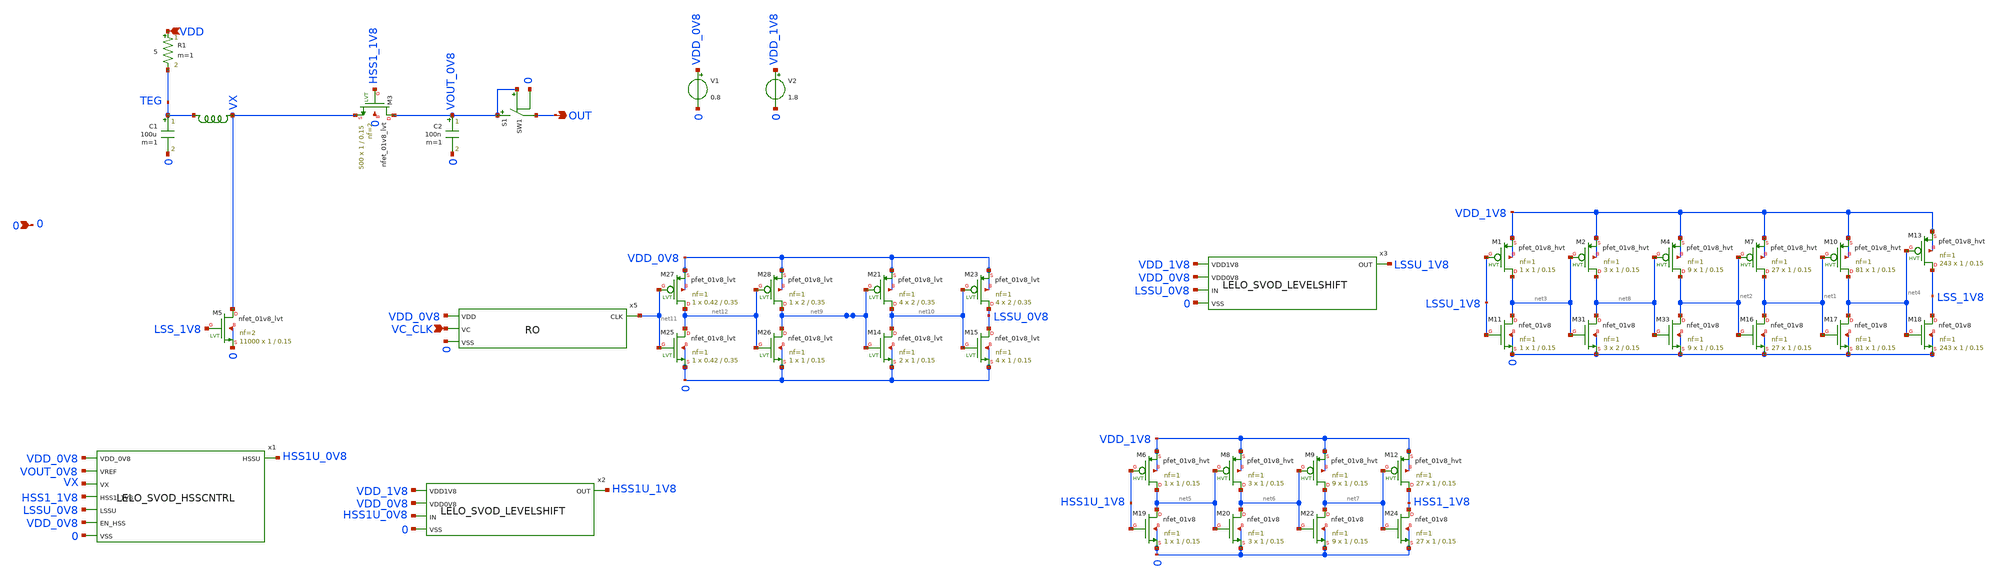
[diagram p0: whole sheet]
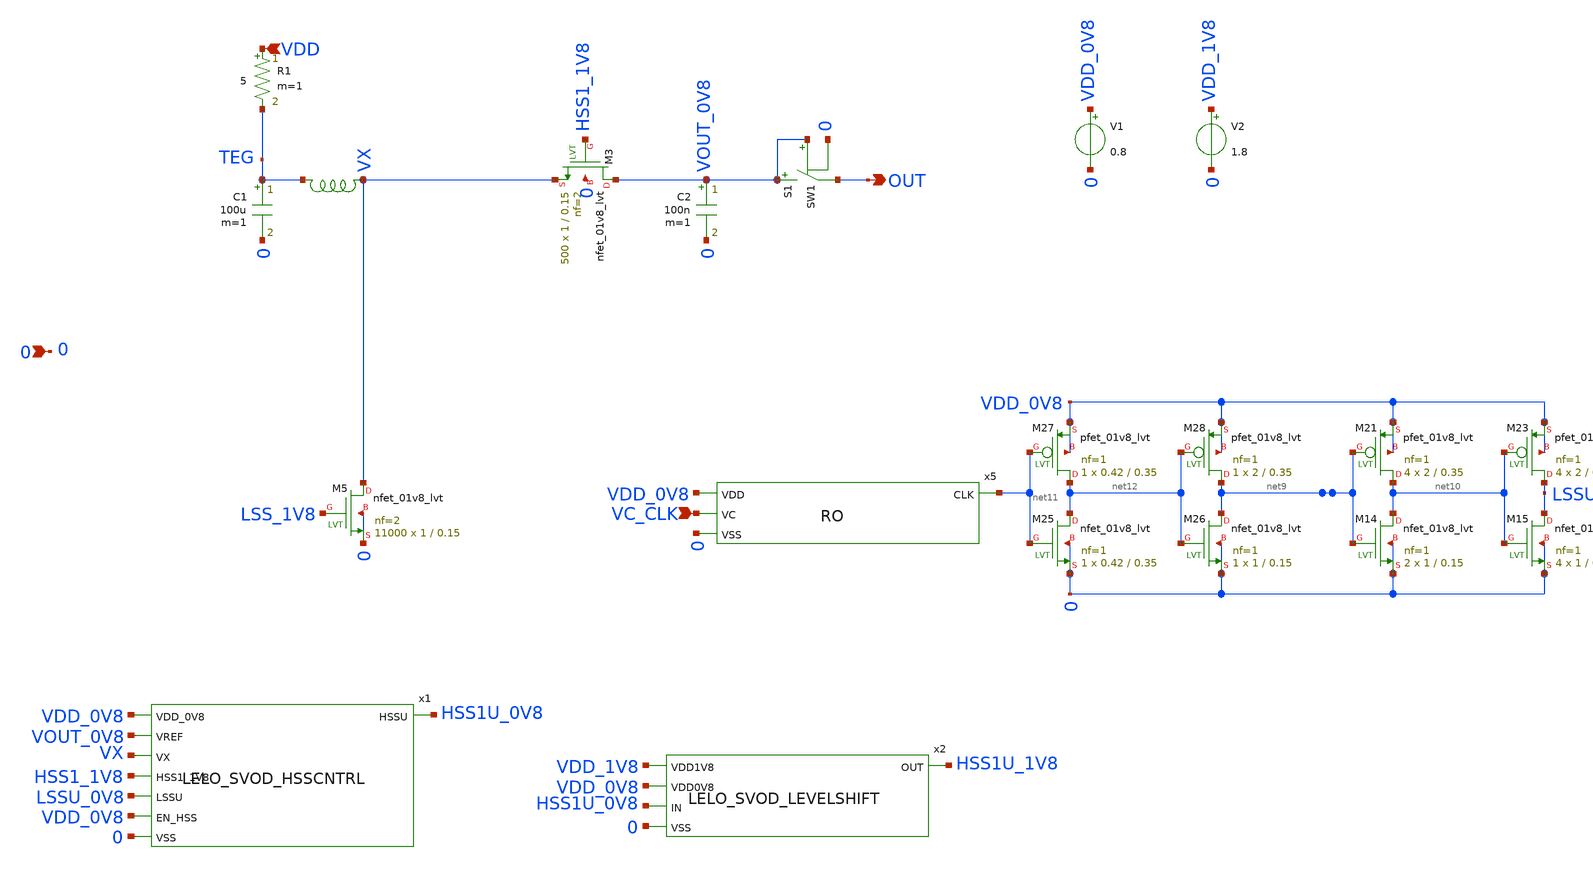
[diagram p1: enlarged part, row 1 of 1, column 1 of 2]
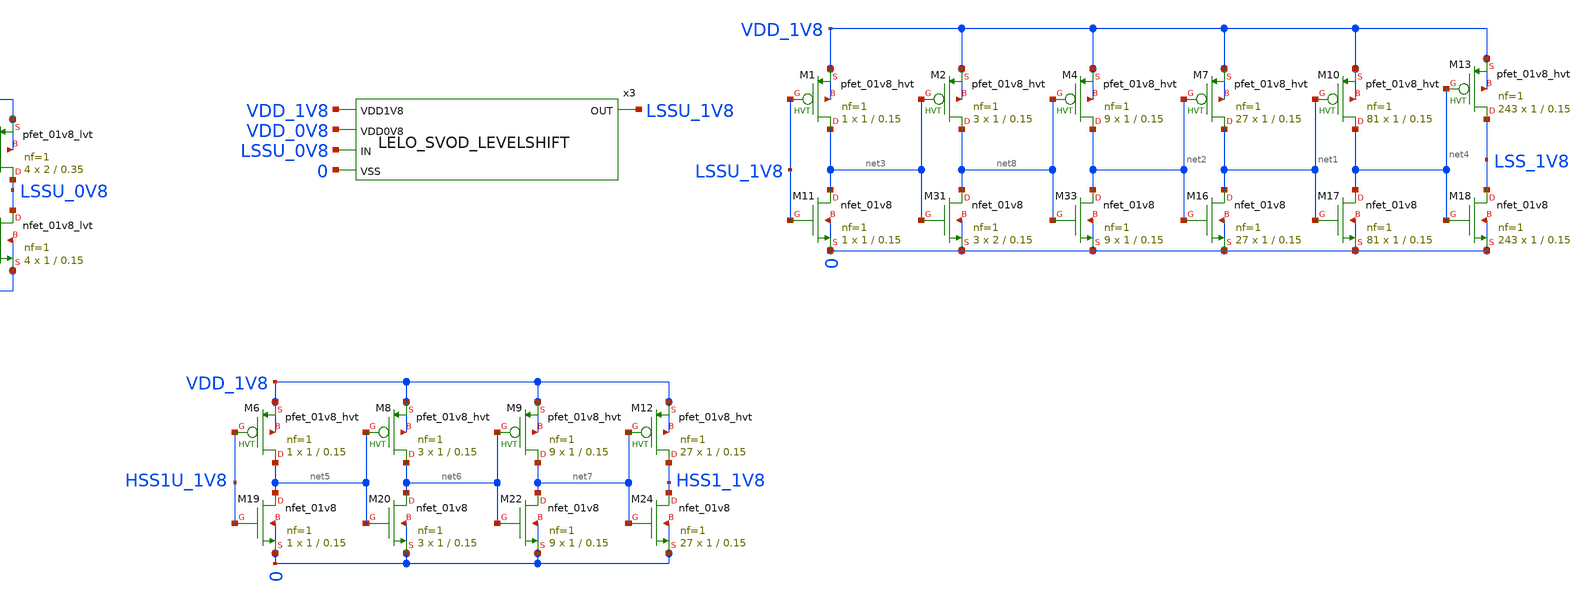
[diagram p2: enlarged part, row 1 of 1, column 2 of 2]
** sch_path: design/LELO_SVOD_SKY130A/LELO_SVOD_0V8_BOOST.sch
**.subckt LELO_SVOD_0V8_BOOST VDD VC_CLK 0 OUT
*.ipin VDD
*.ipin VC_CLK
*.ipin 0
*.opin OUT
R1 VDD TEG 5 m=1
x5 net11 VDD_0V8 VC_CLK 0 RO
C1 TEG 0 100u m=1
XM5 VX LSS_1V8 0 0 sky130_fd_pr__nfet_01v8_lvt L=0.15 W=1 nf=2 ad='int((2 + 1)/2) * 1 / 2 * 0.29' as='int((2 + 2)/2) * 1 / 2 * 0.29'
+ pd='2*int((2 + 1)/2) * (1 / 2 + 0.29)' ps='2*int((2 + 2)/2) * (1 / 2 + 0.29)' nrd='0.29 / 1 ' nrs='0.29 / 1 '
+ sa=0 sb=0 sd=0 mult=11000 m=11000
C2 VOUT_0V8 0 100n m=1
XM11 net3 LSSU_1V8 0 0 sky130_fd_pr__nfet_01v8 L=0.15 W=1 nf=1 ad='int((1 + 1)/2) * 1 / 1 * 0.29' as='int((1 + 2)/2) * 1 / 1 * 0.29'
+ pd='2*int((1 + 1)/2) * (1 / 1 + 0.29)' ps='2*int((1 + 2)/2) * (1 / 1 + 0.29)' nrd='0.29 / 1 ' nrs='0.29 / 1 '
+ sa=0 sb=0 sd=0 mult=1 m=1
XM16 net1 net2 0 0 sky130_fd_pr__nfet_01v8 L=0.15 W=1 nf=1 ad='int((1 + 1)/2) * 1 / 1 * 0.29' as='int((1 + 2)/2) * 1 / 1 * 0.29'
+ pd='2*int((1 + 1)/2) * (1 / 1 + 0.29)' ps='2*int((1 + 2)/2) * (1 / 1 + 0.29)' nrd='0.29 / 1 ' nrs='0.29 / 1 '
+ sa=0 sb=0 sd=0 mult=27 m=27
XM17 net4 net1 0 0 sky130_fd_pr__nfet_01v8 L=0.15 W=1 nf=1 ad='int((1 + 1)/2) * 1 / 1 * 0.29' as='int((1 + 2)/2) * 1 / 1 * 0.29'
+ pd='2*int((1 + 1)/2) * (1 / 1 + 0.29)' ps='2*int((1 + 2)/2) * (1 / 1 + 0.29)' nrd='0.29 / 1 ' nrs='0.29 / 1 '
+ sa=0 sb=0 sd=0 mult=81 m=81
XM18 LSS_1V8 net4 0 0 sky130_fd_pr__nfet_01v8 L=0.15 W=1 nf=1 ad='int((1 + 1)/2) * 1 / 1 * 0.29' as='int((1 + 2)/2) * 1 / 1 * 0.29'
+ pd='2*int((1 + 1)/2) * (1 / 1 + 0.29)' ps='2*int((1 + 2)/2) * (1 / 1 + 0.29)' nrd='0.29 / 1 ' nrs='0.29 / 1 '
+ sa=0 sb=0 sd=0 mult=243 m=243
XM19 net5 HSS1U_1V8 0 0 sky130_fd_pr__nfet_01v8 L=0.15 W=1 nf=1 ad='int((1 + 1)/2) * 1 / 1 * 0.29' as='int((1 + 2)/2) * 1 / 1 * 0.29'
+ pd='2*int((1 + 1)/2) * (1 / 1 + 0.29)' ps='2*int((1 + 2)/2) * (1 / 1 + 0.29)' nrd='0.29 / 1 ' nrs='0.29 / 1 '
+ sa=0 sb=0 sd=0 mult=1 m=1
XM20 net6 net5 0 0 sky130_fd_pr__nfet_01v8 L=0.15 W=1 nf=1 ad='int((1 + 1)/2) * 1 / 1 * 0.29' as='int((1 + 2)/2) * 1 / 1 * 0.29'
+ pd='2*int((1 + 1)/2) * (1 / 1 + 0.29)' ps='2*int((1 + 2)/2) * (1 / 1 + 0.29)' nrd='0.29 / 1 ' nrs='0.29 / 1 '
+ sa=0 sb=0 sd=0 mult=3 m=3
XM22 net7 net6 0 0 sky130_fd_pr__nfet_01v8 L=0.15 W=1 nf=1 ad='int((1 + 1)/2) * 1 / 1 * 0.29' as='int((1 + 2)/2) * 1 / 1 * 0.29'
+ pd='2*int((1 + 1)/2) * (1 / 1 + 0.29)' ps='2*int((1 + 2)/2) * (1 / 1 + 0.29)' nrd='0.29 / 1 ' nrs='0.29 / 1 '
+ sa=0 sb=0 sd=0 mult=9 m=9
XM24 HSS1_1V8 net7 0 0 sky130_fd_pr__nfet_01v8 L=0.15 W=1 nf=1 ad='int((1 + 1)/2) * 1 / 1 * 0.29' as='int((1 + 2)/2) * 1 / 1 * 0.29'
+ pd='2*int((1 + 1)/2) * (1 / 1 + 0.29)' ps='2*int((1 + 2)/2) * (1 / 1 + 0.29)' nrd='0.29 / 1 ' nrs='0.29 / 1 '
+ sa=0 sb=0 sd=0 mult=27 m=27
XM31 net8 net3 0 0 sky130_fd_pr__nfet_01v8 L=0.15 W=2 nf=1 ad='int((1 + 1)/2) * 2 / 1 * 0.29' as='int((1 + 2)/2) * 2 / 1 * 0.29'
+ pd='2*int((1 + 1)/2) * (2 / 1 + 0.29)' ps='2*int((1 + 2)/2) * (2 / 1 + 0.29)' nrd='0.29 / 2 ' nrs='0.29 / 2 '
+ sa=0 sb=0 sd=0 mult=3 m=3
XM33 net2 net8 0 0 sky130_fd_pr__nfet_01v8 L=0.15 W=1 nf=1 ad='int((1 + 1)/2) * 1 / 1 * 0.29' as='int((1 + 2)/2) * 1 / 1 * 0.29'
+ pd='2*int((1 + 1)/2) * (1 / 1 + 0.29)' ps='2*int((1 + 2)/2) * (1 / 1 + 0.29)' nrd='0.29 / 1 ' nrs='0.29 / 1 '
+ sa=0 sb=0 sd=0 mult=9 m=9
x7 TEG VX XGL6030-822_sat
XM3 VOUT_0V8 HSS1_1V8 VX 0 sky130_fd_pr__nfet_01v8_lvt L=0.15 W=1 nf=2 ad='int((2 + 1)/2) * 1 / 2 * 0.29'
+ as='int((2 + 2)/2) * 1 / 2 * 0.29' pd='2*int((2 + 1)/2) * (1 / 2 + 0.29)' ps='2*int((2 + 2)/2) * (1 / 2 + 0.29)'
+ nrd='0.29 / 1 ' nrs='0.29 / 1 ' sa=0 sb=0 sd=0 mult=500 m=500
x1 VDD_0V8 HSS1U_0V8 VOUT_0V8 VX HSS1_1V8 LSSU_0V8 VDD_0V8 0 LELO_SVOD_HSSCNTRL
x2 VDD_1V8 HSS1U_1V8 VDD_0V8 HSS1U_0V8 0 LELO_SVOD_LEVELSHIFT
x3 VDD_1V8 LSSU_1V8 VDD_0V8 LSSU_0V8 0 LELO_SVOD_LEVELSHIFT
XM6 net5 HSS1U_1V8 VDD_1V8 VDD_1V8 sky130_fd_pr__pfet_01v8_hvt L=0.15 W=1 nf=1 ad='int((1 + 1)/2) * 1 / 1 * 0.29'
+ as='int((1 + 2)/2) * 1 / 1 * 0.29' pd='2*int((1 + 1)/2) * (1 / 1 + 0.29)' ps='2*int((1 + 2)/2) * (1 / 1 + 0.29)'
+ nrd='0.29 / 1 ' nrs='0.29 / 1 ' sa=0 sb=0 sd=0 mult=1 m=1
XM8 net6 net5 VDD_1V8 VDD_1V8 sky130_fd_pr__pfet_01v8_hvt L=0.15 W=1 nf=1 ad='int((1 + 1)/2) * 1 / 1 * 0.29'
+ as='int((1 + 2)/2) * 1 / 1 * 0.29' pd='2*int((1 + 1)/2) * (1 / 1 + 0.29)' ps='2*int((1 + 2)/2) * (1 / 1 + 0.29)'
+ nrd='0.29 / 1 ' nrs='0.29 / 1 ' sa=0 sb=0 sd=0 mult=3 m=3
XM9 net7 net6 VDD_1V8 VDD_1V8 sky130_fd_pr__pfet_01v8_hvt L=0.15 W=1 nf=1 ad='int((1 + 1)/2) * 1 / 1 * 0.29'
+ as='int((1 + 2)/2) * 1 / 1 * 0.29' pd='2*int((1 + 1)/2) * (1 / 1 + 0.29)' ps='2*int((1 + 2)/2) * (1 / 1 + 0.29)'
+ nrd='0.29 / 1 ' nrs='0.29 / 1 ' sa=0 sb=0 sd=0 mult=9 m=9
XM12 HSS1_1V8 net7 VDD_1V8 VDD_1V8 sky130_fd_pr__pfet_01v8_hvt L=0.15 W=1 nf=1 ad='int((1 + 1)/2) * 1 / 1 * 0.29'
+ as='int((1 + 2)/2) * 1 / 1 * 0.29' pd='2*int((1 + 1)/2) * (1 / 1 + 0.29)' ps='2*int((1 + 2)/2) * (1 / 1 + 0.29)'
+ nrd='0.29 / 1 ' nrs='0.29 / 1 ' sa=0 sb=0 sd=0 mult=27 m=27
XM1 net3 LSSU_1V8 VDD_1V8 VDD_1V8 sky130_fd_pr__pfet_01v8_hvt L=0.15 W=1 nf=1 ad='int((1 + 1)/2) * 1 / 1 * 0.29'
+ as='int((1 + 2)/2) * 1 / 1 * 0.29' pd='2*int((1 + 1)/2) * (1 / 1 + 0.29)' ps='2*int((1 + 2)/2) * (1 / 1 + 0.29)'
+ nrd='0.29 / 1 ' nrs='0.29 / 1 ' sa=0 sb=0 sd=0 mult=1 m=1
XM2 net8 net3 VDD_1V8 VDD_1V8 sky130_fd_pr__pfet_01v8_hvt L=0.15 W=1 nf=1 ad='int((1 + 1)/2) * 1 / 1 * 0.29'
+ as='int((1 + 2)/2) * 1 / 1 * 0.29' pd='2*int((1 + 1)/2) * (1 / 1 + 0.29)' ps='2*int((1 + 2)/2) * (1 / 1 + 0.29)'
+ nrd='0.29 / 1 ' nrs='0.29 / 1 ' sa=0 sb=0 sd=0 mult=3 m=3
XM4 net2 net8 VDD_1V8 VDD_1V8 sky130_fd_pr__pfet_01v8_hvt L=0.15 W=1 nf=1 ad='int((1 + 1)/2) * 1 / 1 * 0.29'
+ as='int((1 + 2)/2) * 1 / 1 * 0.29' pd='2*int((1 + 1)/2) * (1 / 1 + 0.29)' ps='2*int((1 + 2)/2) * (1 / 1 + 0.29)'
+ nrd='0.29 / 1 ' nrs='0.29 / 1 ' sa=0 sb=0 sd=0 mult=9 m=9
XM7 net1 net2 VDD_1V8 VDD_1V8 sky130_fd_pr__pfet_01v8_hvt L=0.15 W=1 nf=1 ad='int((1 + 1)/2) * 1 / 1 * 0.29'
+ as='int((1 + 2)/2) * 1 / 1 * 0.29' pd='2*int((1 + 1)/2) * (1 / 1 + 0.29)' ps='2*int((1 + 2)/2) * (1 / 1 + 0.29)'
+ nrd='0.29 / 1 ' nrs='0.29 / 1 ' sa=0 sb=0 sd=0 mult=27 m=27
XM10 net4 net1 VDD_1V8 VDD_1V8 sky130_fd_pr__pfet_01v8_hvt L=0.15 W=1 nf=1 ad='int((1 + 1)/2) * 1 / 1 * 0.29'
+ as='int((1 + 2)/2) * 1 / 1 * 0.29' pd='2*int((1 + 1)/2) * (1 / 1 + 0.29)' ps='2*int((1 + 2)/2) * (1 / 1 + 0.29)'
+ nrd='0.29 / 1 ' nrs='0.29 / 1 ' sa=0 sb=0 sd=0 mult=81 m=81
XM13 LSS_1V8 net4 VDD_1V8 VDD_1V8 sky130_fd_pr__pfet_01v8_hvt L=0.15 W=1 nf=1 ad='int((1 + 1)/2) * 1 / 1 * 0.29'
+ as='int((1 + 2)/2) * 1 / 1 * 0.29' pd='2*int((1 + 1)/2) * (1 / 1 + 0.29)' ps='2*int((1 + 2)/2) * (1 / 1 + 0.29)'
+ nrd='0.29 / 1 ' nrs='0.29 / 1 ' sa=0 sb=0 sd=0 mult=243 m=243
V1 VDD_0V8 0 0.8
V2 VDD_1V8 0 1.8
S1 VOUT_0V8 OUT VOUT_0V8 0 SW1
XM14 net10 net9 0 0 sky130_fd_pr__nfet_01v8_lvt L=0.15 W=1 nf=1 ad='int((1 + 1)/2) * 1 / 1 * 0.29' as='int((1 + 2)/2) * 1 / 1 * 0.29'
+ pd='2*int((1 + 1)/2) * (1 / 1 + 0.29)' ps='2*int((1 + 2)/2) * (1 / 1 + 0.29)' nrd='0.29 / 1 ' nrs='0.29 / 1 '
+ sa=0 sb=0 sd=0 mult=2 m=2
XM15 LSSU_0V8 net10 0 0 sky130_fd_pr__nfet_01v8_lvt L=0.15 W=1 nf=1 ad='int((1 + 1)/2) * 1 / 1 * 0.29'
+ as='int((1 + 2)/2) * 1 / 1 * 0.29' pd='2*int((1 + 1)/2) * (1 / 1 + 0.29)' ps='2*int((1 + 2)/2) * (1 / 1 + 0.29)'
+ nrd='0.29 / 1 ' nrs='0.29 / 1 ' sa=0 sb=0 sd=0 mult=4 m=4
XM21 net10 net9 VDD_0V8 VDD_0V8 sky130_fd_pr__pfet_01v8_lvt L=0.35 W=2 nf=1 ad='int((1 + 1)/2) * 2 / 1 * 0.29'
+ as='int((1 + 2)/2) * 2 / 1 * 0.29' pd='2*int((1 + 1)/2) * (2 / 1 + 0.29)' ps='2*int((1 + 2)/2) * (2 / 1 + 0.29)'
+ nrd='0.29 / 2 ' nrs='0.29 / 2 ' sa=0 sb=0 sd=0 mult=4 m=4
XM23 LSSU_0V8 net10 VDD_0V8 VDD_0V8 sky130_fd_pr__pfet_01v8_lvt L=0.35 W=2 nf=1 ad='int((1 + 1)/2) * 2 / 1 * 0.29'
+ as='int((1 + 2)/2) * 2 / 1 * 0.29' pd='2*int((1 + 1)/2) * (2 / 1 + 0.29)' ps='2*int((1 + 2)/2) * (2 / 1 + 0.29)'
+ nrd='0.29 / 2 ' nrs='0.29 / 2 ' sa=0 sb=0 sd=0 mult=4 m=4
XM25 net12 net11 0 0 sky130_fd_pr__nfet_01v8_lvt L=0.35 W=0.42 nf=1 ad='int((1 + 1)/2) * 0.42 / 1 * 0.29'
+ as='int((1 + 2)/2) * 0.42 / 1 * 0.29' pd='2*int((1 + 1)/2) * (0.42 / 1 + 0.29)' ps='2*int((1 + 2)/2) * (0.42 / 1 + 0.29)'
+ nrd='0.29 / 0.42 ' nrs='0.29 / 0.42 ' sa=0 sb=0 sd=0 mult=1 m=1
XM26 net9 net12 0 0 sky130_fd_pr__nfet_01v8_lvt L=0.15 W=1 nf=1 ad='int((1 + 1)/2) * 1 / 1 * 0.29' as='int((1 + 2)/2) * 1 / 1 * 0.29'
+ pd='2*int((1 + 1)/2) * (1 / 1 + 0.29)' ps='2*int((1 + 2)/2) * (1 / 1 + 0.29)' nrd='0.29 / 1 ' nrs='0.29 / 1 '
+ sa=0 sb=0 sd=0 mult=1 m=1
XM27 net12 net11 VDD_0V8 VDD_0V8 sky130_fd_pr__pfet_01v8_lvt L=0.35 W=0.42 nf=1 ad='int((1 + 1)/2) * 0.42 / 1 * 0.29'
+ as='int((1 + 2)/2) * 0.42 / 1 * 0.29' pd='2*int((1 + 1)/2) * (0.42 / 1 + 0.29)' ps='2*int((1 + 2)/2) * (0.42 / 1 + 0.29)'
+ nrd='0.29 / 0.42 ' nrs='0.29 / 0.42 ' sa=0 sb=0 sd=0 mult=1 m=1
XM28 net9 net12 VDD_0V8 VDD_0V8 sky130_fd_pr__pfet_01v8_lvt L=0.35 W=2 nf=1 ad='int((1 + 1)/2) * 2 / 1 * 0.29'
+ as='int((1 + 2)/2) * 2 / 1 * 0.29' pd='2*int((1 + 1)/2) * (2 / 1 + 0.29)' ps='2*int((1 + 2)/2) * (2 / 1 + 0.29)'
+ nrd='0.29 / 2 ' nrs='0.29 / 2 ' sa=0 sb=0 sd=0 mult=1 m=1
**.ends
**** begin user architecture code
.MODEL SW1 SW   VT=0.8 VH=0.001  RON=0.001 ROFF=10G
**** end user architecture code
.end
